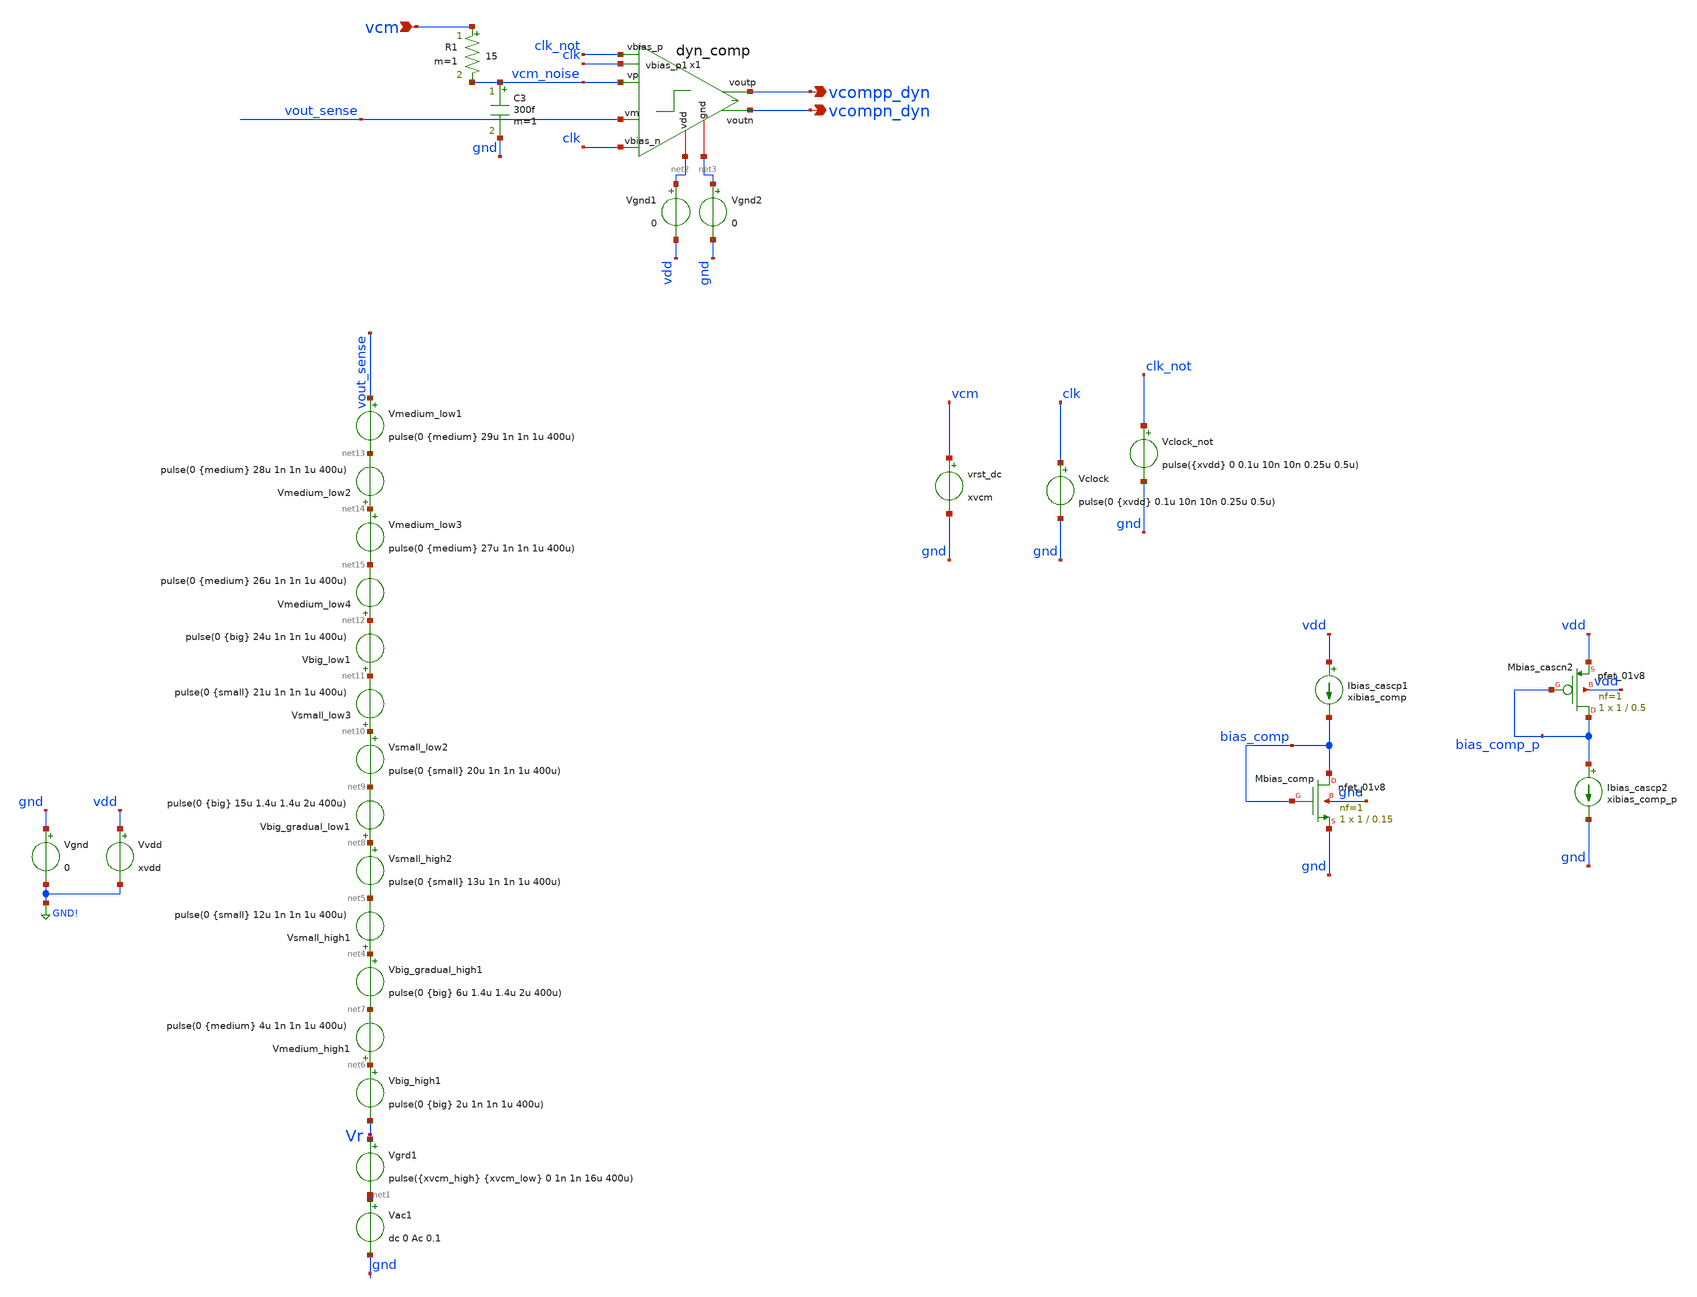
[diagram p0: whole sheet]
** sch_path: analog/xschem/test_comp.sch
**.subckt test_comp vcm vcompp_dyn vcompn_dyn
*.ipin vcm
*.opin vcompp_dyn
*.opin vcompn_dyn
Vgnd gnd GND! 0
Vvdd vdd GND! xvdd
vrst_dc vcm gnd xvcm
Ibias_cascp1 vdd bias_comp xibias_comp
XMbias_comp bias_comp bias_comp gnd gnd sky130_fd_pr__nfet_01v8 L=0.15 W=1 nf=1 ad='int((1 + 1)/2) * 1 / 1 * 0.29'
+ as='int((1 + 2)/2) * 1 / 1 * 0.29' pd='2*int((1 + 1)/2) * (1 / 1 + 0.29)' ps='2*int((1 + 2)/2) * (1 / 1 + 0.29)'
+ nrd='0.29 / 1 ' nrs='0.29 / 1 ' sa=0 sb=0 sd=0 mult=1 m=1
Ibias_cascp2 bias_comp_p gnd xibias_comp_p
XMbias_cascn2 bias_comp_p bias_comp_p vdd vdd sky130_fd_pr__pfet_01v8 L=0.5 W=1 nf=1 ad='int((1 + 1)/2) * 1 / 1 * 0.29'
+ as='int((1 + 2)/2) * 1 / 1 * 0.29' pd='2*int((1 + 1)/2) * (1 / 1 + 0.29)' ps='2*int((1 + 2)/2) * (1 / 1 + 0.29)'
+ nrd='0.29 / 1 ' nrs='0.29 / 1 ' sa=0 sb=0 sd=0 mult=1 m=1
Vclock clk gnd pulse(0 {xvdd} 0.1u 10n 10n 0.25u 0.5u)
Vclock_not clk_not gnd pulse({xvdd} 0 0.1u 10n 10n 0.25u 0.5u)
Vsmall_high1 net4 net5 pulse(0 {small} 12u 1n 1n 1u 400u)
Vbig_high1 net6 Vr pulse(0 {big} 2u 1n 1n 1u 400u)
Vbig_gradual_high1 net4 net7 pulse(0 {big} 6u 1.4u 1.4u 2u 400u)
Vbig_gradual_low1 net8 net9 pulse(0 {big} 15u 1.4u 1.4u 2u 400u)
Vsmall_low2 net10 net9 pulse(0 {small} 20u 1n 1n 1u 400u)
Vgrd1 Vr net1 pulse({xvcm_high} {xvcm_low} 0 1n 1n 16u 400u)
Vbig_low1 net11 net12 pulse(0 {big} 24u 1n 1n 1u 400u)
Vmedium_high1 net6 net7 pulse(0 {medium} 4u 1n 1n 1u 400u)
Vmedium_low1 vout_sense net13 pulse(0 {medium} 29u 1n 1n 1u 400u)
Vac1 net1 gnd dc 0 Ac 0.1
Vsmall_high2 net8 net5 pulse(0 {small} 13u 1n 1n 1u 400u)
Vsmall_low3 net10 net11 pulse(0 {small} 21u 1n 1n 1u 400u)
Vmedium_low2 net14 net13 pulse(0 {medium} 28u 1n 1n 1u 400u)
Vmedium_low3 net14 net15 pulse(0 {medium} 27u 1n 1n 1u 400u)
Vmedium_low4 net12 net15 pulse(0 {medium} 26u 1n 1n 1u 400u)
Vgnd1 net2 vdd 0
Vgnd2 net3 gnd 0
x1 net2 vcm_noise vout_sense net3 clk_not clk vcompp_dyn vcompn_dyn clk dyn_comp
R1 vcm vcm_noise 15 m=1
C3 vcm_noise gnd 300f m=1
**** begin user architecture code

** opencircuitdesign pdks install
.lib $::SKYWATER_MODELS/sky130.lib.spice tt



.option reltol=1e-6 abstol=1e-15 vntol=1e-9 gmin=1e-15
.option trtol=5 chgtol=1e-16

.param big = 0.08
.param medium = 0.01
.param small = 0.002
.param xvcm = 0.9
.param xvcm_low = {xvcm - 0.001}
.param xvcm_high = {xvcm + 0.001}
.param xipd = 1e-9
.param xvph_bias = 1.5
.param xisf_bias = 9.2n
.param xvcascn = 0.2
.param xvcascp = 1.6
.param xicol_bias = 5e-7
.param xvtail = 0.5
.param xvdd = 1.8
.param xibias_cascp = 50n
.param xibias_cascn = 50n
.param xibias_comp = 50n
.param xibias_comp_p = 50n


.control
* plot v(vout_sense)
save v(vout_sense)
save v(vcomp)
let vnoise_in = v(vcm_noise) - v(vcm)
save all
tran .1n 30u
*ac dec 20 1 1e10

* save v(vphoto) v(vph_sf) v(vin) v(sense) v(feedback) v(vcomp)
* save v(pix_rst) v(vout) v(pbchk) v(vref) v(row_sel) v(lrst)
* save v(vcompp_dyn) v(vcompn_dyn)
*plot db20(v(vcompp_dyn_v2)/v(Vr))
*ic v(vin)=0.6
*ic v(vout)=1
* dc vph 0 1.8 10m
*save all
* op
write test_comp.raw
.endc

*plot db(v(vcompp_dyn_v2) 180*cph(v(vcompp_dyn_2))/pi



**** end user architecture code
**.ends
.GLOBAL GND!
.end
